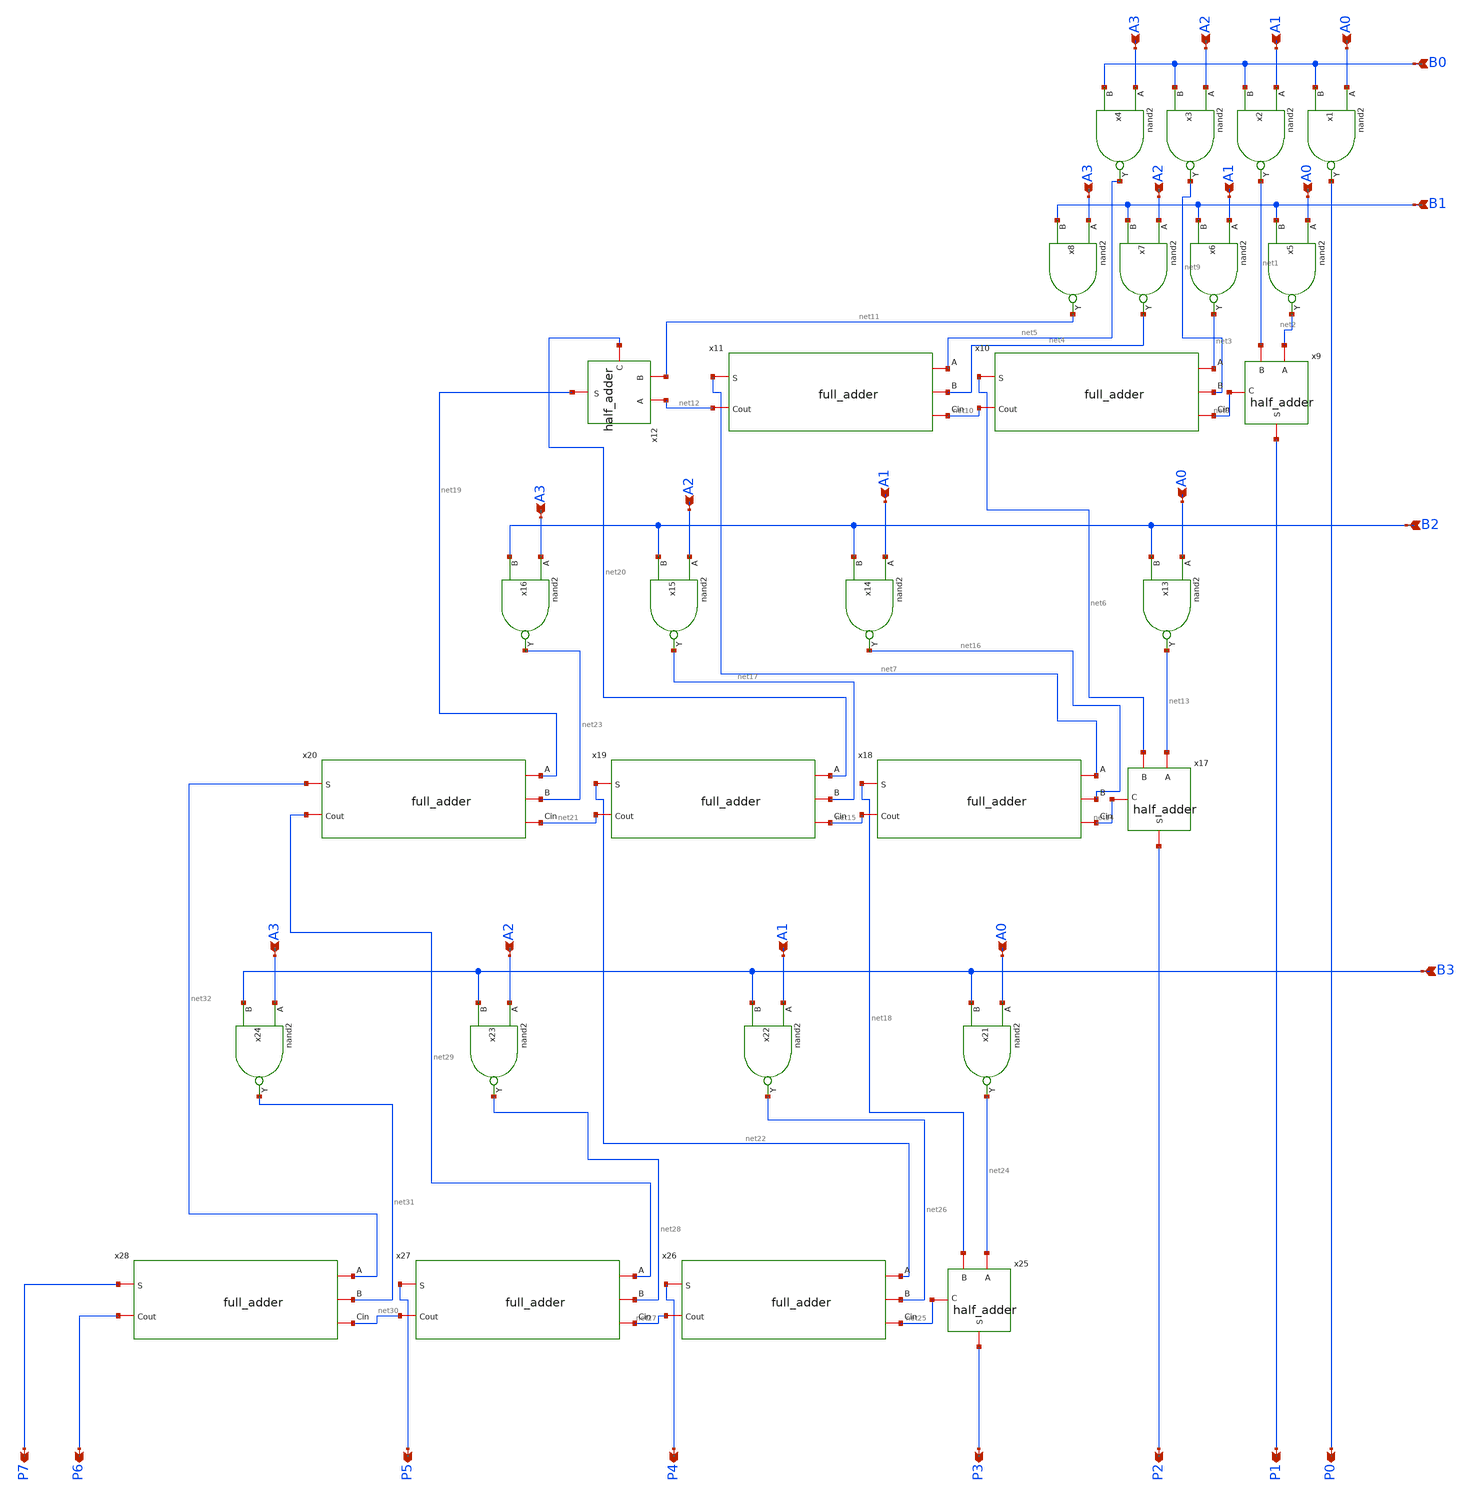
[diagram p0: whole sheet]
** sch_path: design/xschem/MULTIPLIER/multiplier.sch
**.subckt multiplier B0 B1 A3 A2 A1 A0 B2 B3 P3 P4 P5 P6 P7 P2 P0 P1 A0 A1 A2 A3 A0 A1 A2 A3 A0 A1
*+ A2 A3
*.ipin B0
*.ipin B1
*.ipin A3
*.ipin A2
*.ipin A1
*.ipin A0
*.ipin B2
*.ipin B3
*.opin P3
*.opin P4
*.opin P5
*.opin P6
*.opin P7
*.opin P2
*.opin P0
*.opin P1
*.ipin A0
*.ipin A1
*.ipin A2
*.ipin A3
*.ipin A0
*.ipin A1
*.ipin A2
*.ipin A3
*.ipin A0
*.ipin A1
*.ipin A2
*.ipin A3
x1 A0 B0 VSS VDD P0 nand2
x2 A1 B0 VSS VDD net1 nand2
x3 A2 B0 VSS VDD net9 nand2
x4 A3 B0 VSS VDD net5 nand2
x5 A0 B1 VSS VDD net2 nand2
x6 A1 B1 VSS VDD net3 nand2
x7 A2 B1 VSS VDD net4 nand2
x8 A3 B1 VSS VDD net11 nand2
x9 net2 P1 net1 net8 VSS VDD half_adder
x10 net3 net6 net9 net8 net10 full_adder
x11 net5 net7 net4 net10 net12 full_adder
x12 net12 net19 net11 net20 VSS VDD half_adder
x13 A0 B2 VSS VDD net13 nand2
x14 A1 B2 VSS VDD net16 nand2
x15 A2 B2 VSS VDD net17 nand2
x16 A3 B2 VSS VDD net23 nand2
x17 net13 P2 net6 net14 VSS VDD half_adder
x18 net7 net18 net16 net14 net15 full_adder
x19 net20 net22 net17 net15 net21 full_adder
x21 A0 B3 VSS VDD net24 nand2
x22 A1 B3 VSS VDD net26 nand2
x23 A2 B3 VSS VDD net28 nand2
x24 A3 B3 VSS VDD net31 nand2
x25 net24 P3 net18 net25 VSS VDD half_adder
x26 net22 P4 net26 net25 net27 full_adder
x27 net29 P5 net28 net27 net30 full_adder
x20 net19 net32 net23 net21 net29 full_adder
x28 net32 P7 net31 net30 P6 full_adder
**.ends
.end
